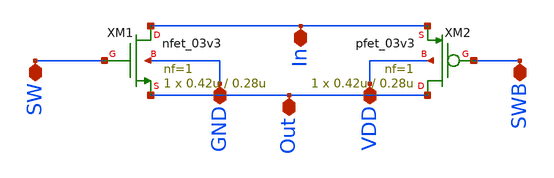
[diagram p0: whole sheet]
** sch_path: src/pixel/TG.sch
**.subckt TG In Out SW GND VDD SWB
*.iopin In
*.iopin Out
*.iopin SW
*.iopin GND
*.iopin VDD
*.iopin SWB
XM1 In SW Out GND nfet_03v3 L=0.28u W=0.42u nf=1 ad='int((nf+1)/2) * W/nf * 0.18u' as='int((nf+2)/2) * W/nf * 0.18u'
+ pd='2*int((nf+1)/2) * (W/nf + 0.18u)' ps='2*int((nf+2)/2) * (W/nf + 0.18u)' nrd='0.18u / W' nrs='0.18u / W'
+ sa=0 sb=0 sd=0 m=1
XM2 Out SWB In VDD pfet_03v3 L=0.28u W=0.42u nf=1 ad='int((nf+1)/2) * W/nf * 0.18u' as='int((nf+2)/2) * W/nf * 0.18u'
+ pd='2*int((nf+1)/2) * (W/nf + 0.18u)' ps='2*int((nf+2)/2) * (W/nf + 0.18u)' nrd='0.18u / W' nrs='0.18u / W'
+ sa=0 sb=0 sd=0 m=1
**.ends
.end
